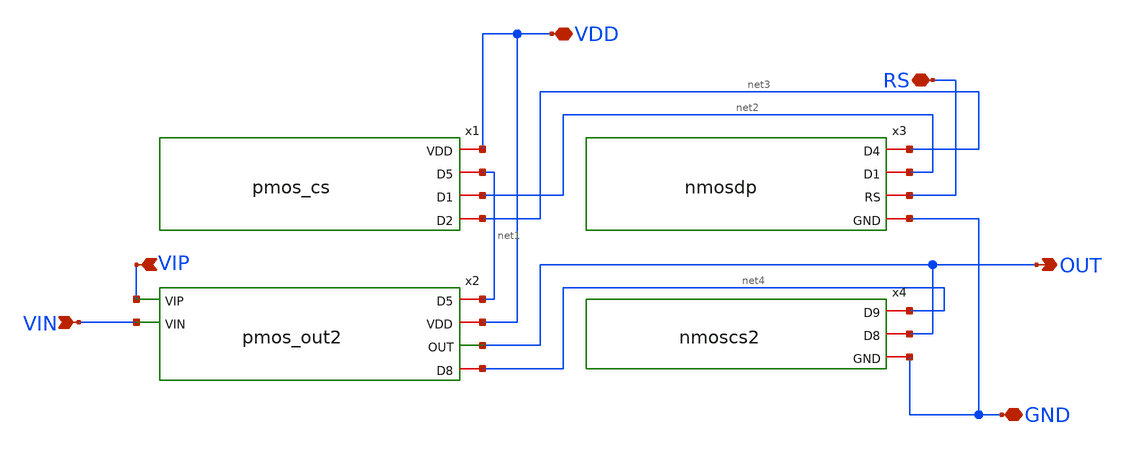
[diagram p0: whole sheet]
** sch_path: xschem/opampfin.sch
**.subckt opampfin VDD VIP VIN RS GND OUT
*.iopin VDD
*.ipin VIP
*.ipin VIN
*.iopin RS
*.iopin GND
*.opin OUT
x1 VDD net1 net2 net3 pmos_cs
x3 net3 net2 RS GND nmosdp
x4 net4 OUT GND nmoscs2
x2 net1 VDD VIP VIN OUT net4 pmos_out2
**.ends
.end
